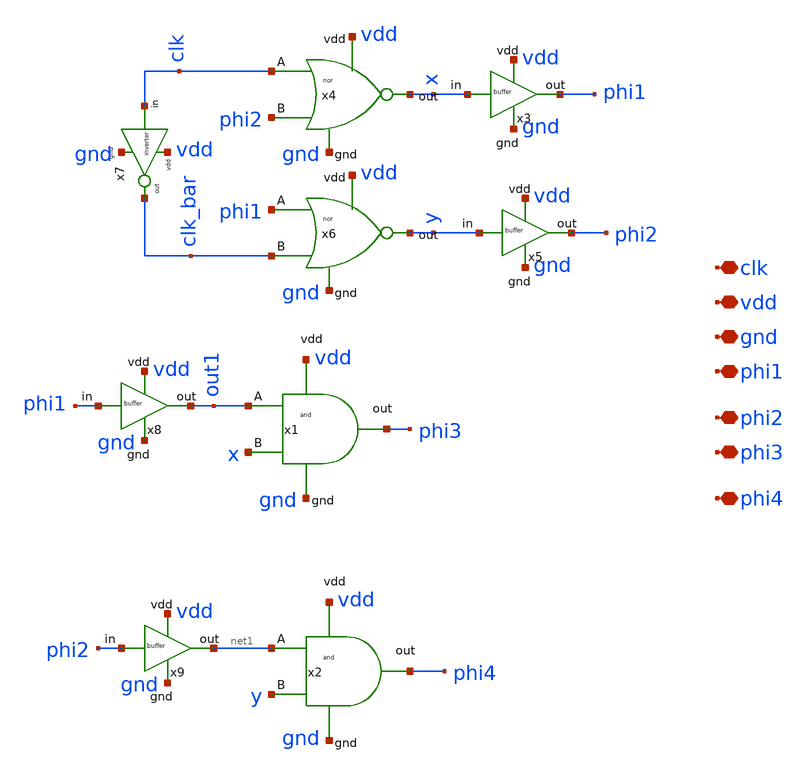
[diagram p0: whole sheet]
** sch_path: dependencies/OTA/OTA-main/schematic/xschem/Clock_gen_using_transistor_hv/pulse_gen_circuit.sch
**.subckt pulse_gen_circuit vdd gnd phi1 phi2 phi3 phi4 clk
*.iopin vdd
*.iopin gnd
*.iopin phi1
*.iopin phi2
*.iopin phi3
*.iopin phi4
*.iopin clk
x1 vdd x out1 gnd phi3 and
x2 vdd y net1 gnd phi4 and
x4 vdd phi2 clk gnd x nor
x6 vdd clk_bar phi1 gnd y nor
x7 clk clk_bar vdd gnd inverter
x8 phi1 out1 vdd gnd buffer
x9 phi2 net1 vdd gnd buffer
x3 x phi1 vdd gnd buffer
x5 y phi2 vdd gnd buffer
**.ends
.end
